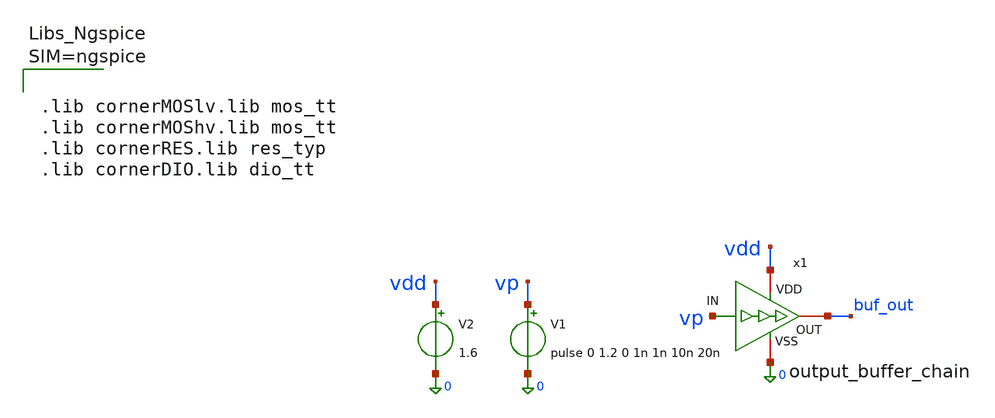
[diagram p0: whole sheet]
** sch_path: analog/output_buffer_chain/testbenches/output_buffer_chain-tb.sch
**.subckt output_buffer_chain-tb
x1 vdd vp buf_out 0 output_buffer_chain
V1 vp 0 pulse 0 1.2 0 1n 1n 10n 20n
V2 vdd 0 1.6
**** begin user architecture code



.lib cornerMOSlv.lib mos_tt
.lib cornerMOShv.lib mos_tt
.lib cornerRES.lib res_typ
.lib cornerDIO.lib dio_tt





.param temp=27
.control
tran 0.2n 100n
* Propagation delay
* input threshold = 0.6 V  (50% of 1.2 V input swing)
* output threshold = 0.8 V (50% of 1.6 V supply)
meas tran tplh trig v(vp)      val=0.6 td=20n rise=1                 targ v(buf_out) val=0.8 td=20n
+ rise=1

meas tran tphl trig v(vp)      val=0.6 td=20n fall=1                 targ v(buf_out) val=0.8 td=20n
+ fall=1

* Output rise / fall time (10%..90% of 1.6 V)
meas tran trise_out trig v(buf_out) val=0.16 td=20n rise=1                      targ v(buf_out)
+ val=1.44 td=20n rise=1

meas tran tfall_out trig v(buf_out) val=1.44 td=20n fall=1                      targ v(buf_out)
+ val=0.16 td=20n fall=1

write output_buffer_chain-tb.raw
.endc


**** end user architecture code
**.ends

* expanding   symbol:  analog/output_buffer_chain/output_buffer_chain.sym # of pins=4
** sym_path: analog/output_buffer_chain/output_buffer_chain.sym
** sch_path: analog/output_buffer_chain/output_buffer_chain.sch
.subckt output_buffer_chain VDD IN OUT VSS
*.ipin IN
*.opin OUT
*.iopin VDD
*.iopin VSS
XM1 net1 IN VSS VSS sg13_lv_nmos w=2.0u l=0.45u ng=1 m=1 mm_ok=1
XM2 VDD IN net1 VDD sg13_lv_pmos w=1.0u l=0.45u ng=1 m=1 mm_ok=1
XM3 net2 net1 VSS VSS sg13_lv_nmos w=4.0u l=0.45u ng=1 m=1 mm_ok=1
XM4 VDD net1 net2 VDD sg13_lv_pmos w=2.0u l=0.45u ng=1 m=1 mm_ok=1
XM5 OUT net2 VSS VSS sg13_lv_nmos w=16.0u l=0.45u ng=2 m=1 mm_ok=1
XM6 VDD net2 OUT VDD sg13_lv_pmos w=8.0u l=0.45u ng=1 m=1 mm_ok=1
.ends

.end
